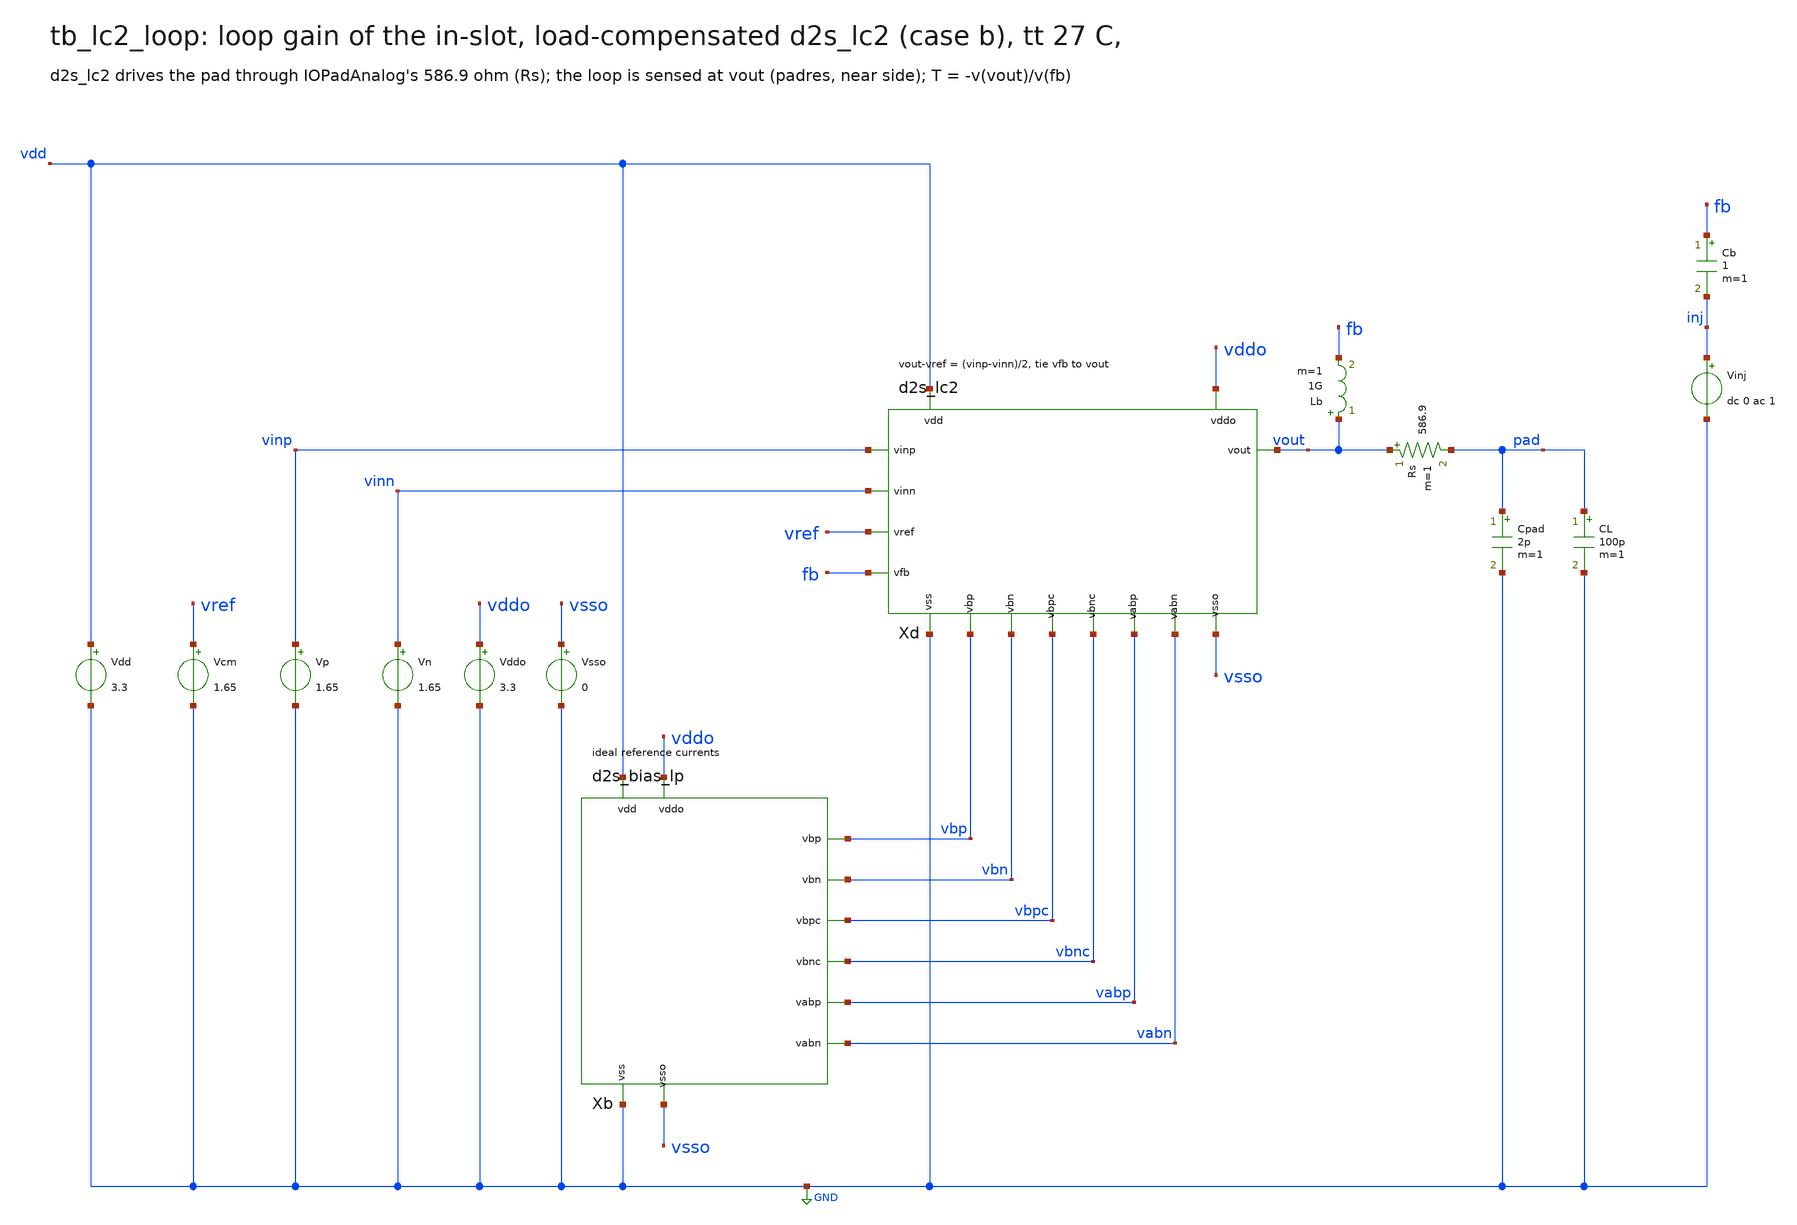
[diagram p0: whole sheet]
** sch_path: sudelbuecher/design_considerations/class_ab_pad_driver/improvements/xschem/tb_lc2_loop.sch
**.subckt tb_lc2_loop
Vdd vdd GND 3.3
Vcm vref GND 1.65
Xb vdd GND vddo vsso vbp vbn vbpc vbnc vabp vabn d2s_bias_lp
Xd vdd GND vddo vsso vinp vinn vref vout fb vbp vbn vbpc vbnc vabp vabn d2s_lc2
Vp vinp GND 1.65
Vn vinn GND 1.65
Rs vout pad 586.9 m=1
Cpad pad GND 2p m=1
CL pad GND 100p m=1
Lb vout fb 1G m=1
Cb fb inj 1 m=1
Vinj inj GND dc 0 ac 1
Vddo vddo GND 3.3
Vsso vsso GND 0
**** begin user architecture code

.lib cornerMOShv.lib mos_tt
.lib cornerRES.lib res_typ
.lib cornerCAP.lib cap_typ
.control
ac dec 50 10 1G
let T=-v(vout)/v(fb)
meas ac T0 find vdb(T) at=10
meas ac fc when vdb(T)=0
meas ac pT find vp(T) when vdb(T)=0
let pm=180/pi*pT+180
print T0 fc pm
if $?batchmode = 0
  plot vdb(T) 180/pi*vp(T)
end
.endc

**** end user architecture code
**.ends

* expanding   symbol:  d2s_bias_lp.sym # of pins=10
** sym_path: sudelbuecher/design_considerations/class_ab_pad_driver/improvements/xschem/d2s_bias_lp.sym
** sch_path: sudelbuecher/design_considerations/class_ab_pad_driver/improvements/xschem/d2s_bias_lp.sch
.subckt d2s_bias_lp vdd vss vddo vsso vbp vbn vbpc vbnc vabp vabn
*.iopin vdd
*.iopin vss
*.iopin vddo
*.iopin vsso
*.opin vbp
*.opin vbn
*.opin vbpc
*.opin vbnc
*.opin vabp
*.opin vabn
XBP vbp vbp vdd vdd sg13_hv_pmos w=5u l=6u ng=1 m=1 mm_ok=1
IBP vbp vss 5u
XBPC vbpc vbpc vdd vdd sg13_hv_pmos w=1u l=4u ng=1 m=1 mm_ok=1
IBPC vbpc vss 2u
XRP1 n1 n1 vddo vddo sg13_hv_pmos w=13.32u l=0.6u ng=2 m=1 mm_ok=1
XRP2 vabp vabp n1 vdd sg13_hv_pmos w=6.66u l=0.6u ng=1 m=1 mm_ok=1
IABP vabp vss 5u
IBN vdd vbn 5u
XBN vbn vbn vss vss sg13_hv_nmos w=6u l=6u ng=1 m=1 mm_ok=1
IBNC vdd vbnc 2u
XBNC vbnc vbnc vss vss sg13_hv_nmos w=1u l=8u ng=1 m=1 mm_ok=1
IABN vdd vabn 5u
XRN2 vabn vabn n2 vss sg13_hv_nmos w=4.4u l=1u ng=1 m=1 mm_ok=1
XRN1 n2 n2 vsso vsso sg13_hv_nmos w=8.8u l=1u ng=2 m=1 mm_ok=1
.ends


* expanding   symbol:  d2s_lc2.sym # of pins=15
** sym_path: sudelbuecher/design_considerations/class_ab_pad_driver/improvements/xschem/d2s_lc2.sym
** sch_path: sudelbuecher/design_considerations/class_ab_pad_driver/improvements/xschem/d2s_lc2.sch
.subckt d2s_lc2 vdd vss vddo vsso vinp vinn vref vout vfb vbp vbn vbpc vbnc vabp vabn
*.iopin vdd
*.iopin vss
*.iopin vddo
*.iopin vsso
*.ipin vinp
*.ipin vinn
*.ipin vref
*.iopin vout
*.ipin vfb
*.ipin vbp
*.ipin vbn
*.ipin vbpc
*.ipin vbnc
*.ipin vabp
*.ipin vabn
XA x y vinp vref vdd vss vbp unit_r2
XB x y vref vinn vdd vss vbp unit_r2
XC1 x y vref vfb vdd vss vbp unit_r2
XC2 x y vref vfb vdd vss vbp unit_r2
XFNL l2 vabn l1 vss sg13_hv_nmos w=4.4u l=1u ng=1 m=1 mm_ok=1
XCX l1 vbnc x vss sg13_hv_nmos w=30u l=3u ng=2 m=1 mm_ok=1
XSX x vbn vss vss sg13_hv_nmos w=36u l=6u ng=4 m=1 mm_ok=1
XPL pl l2 vdd vdd sg13_hv_pmos w=24u l=4u ng=4 m=1 mm_ok=1
XPCL l2 vbpc pl vdd sg13_hv_pmos w=30u l=3u ng=2 m=1 mm_ok=1
XFPL l1 vabp l2 vdd sg13_hv_pmos w=6.66u l=0.6u ng=1 m=1 mm_ok=1
XPR pr l2 vdd vdd sg13_hv_pmos w=24u l=4u ng=4 m=1 mm_ok=1
XPCR a vbpc pr vdd sg13_hv_pmos w=30u l=3u ng=2 m=1 mm_ok=1
XABP b vabp a vdd sg13_hv_pmos w=6.66u l=0.6u ng=1 m=1 mm_ok=1
XABN a vabn b vss sg13_hv_nmos w=4.4u l=1u ng=1 m=1 mm_ok=1
XCY b vbnc y vss sg13_hv_nmos w=30u l=3u ng=2 m=1 mm_ok=1
XSY y vbn vss vss sg13_hv_nmos w=36u l=6u ng=4 m=1 mm_ok=1
XOP op a vddo vddo sg13_hv_pmos w=273.06u l=0.6u ng=41 m=1 mm_ok=1
XOPC vout vref op op sg13_hv_pmos w=273.06u l=0.6u ng=41 m=1 mm_ok=1
XONC vout vref on vsso sg13_hv_nmos w=145.2u l=0.6u ng=33 m=1 mm_ok=1
XON on b vsso vsso sg13_hv_nmos w=145.2u l=1u ng=33 m=1 mm_ok=1
XDP a a vddo vddo sg13_hv_pmos w=6.66u l=0.6u ng=1 m=1 mm_ok=1
XDN b b vsso vsso sg13_hv_nmos w=3.8u l=1u ng=1 m=1 mm_ok=1
.ends


* expanding   symbol:  unit_r2.sym # of pins=7
** sym_path: sudelbuecher/design_considerations/class_ab_pad_driver/improvements/xschem/unit_r2.sym
** sch_path: sudelbuecher/design_considerations/class_ab_pad_driver/improvements/xschem/unit_r2.sch
.subckt unit_r2 x y gp gn vdd vss vbp
*.opin x
*.opin y
*.ipin gp
*.ipin gn
*.iopin vdd
*.iopin vss
*.ipin vbp
XTa sa vbp vdd vdd sg13_hv_pmos w=5u l=6u ng=1 m=1 mm_ok=1
XTb sb vbp vdd vdd sg13_hv_pmos w=5u l=6u ng=1 m=1 mm_ok=1
XMa y gp sa sa sg13_hv_pmos w=20u l=1u ng=2 m=1 mm_ok=1
XMb x gn sb sb sg13_hv_pmos w=20u l=1u ng=2 m=1 mm_ok=1
XR sa sb vss rhigh w=0.5u l=50.6u m=1 b=0 mm_ok=1
.ends

.GLOBAL GND
.end
